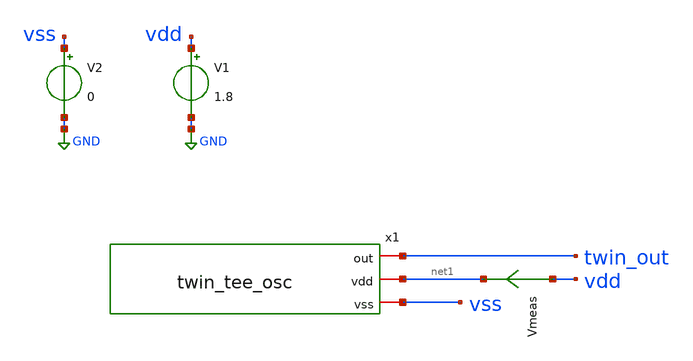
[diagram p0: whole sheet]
** sch_path: xschem/tb_twin_tee_osc.sch
**.subckt tb_twin_tee_osc
V1 vdd GND 1.8
V2 vss GND 0
x1 twin_out net1 vss twin_tee_osc
Vmeas vdd net1 0
**** begin user architecture code

** opencircuitdesign pdks install
.lib $::SKYWATER_MODELS/sky130.lib.spice tt_mm
*.include $::SKYWATER_STDCELLS/sky130_fd_sc_hd.spice





*.option  METHOD = GEAR
*.param mc_mm_switch=0
*.ic v(twin_out)=0.8
.control
repeat 5

  tran 500p 5u uic
  write tb_twin_tee_osc.raw
  set appendwrite
  reset

end
.endc



**** end user architecture code
**.ends
.GLOBAL GND
.end
